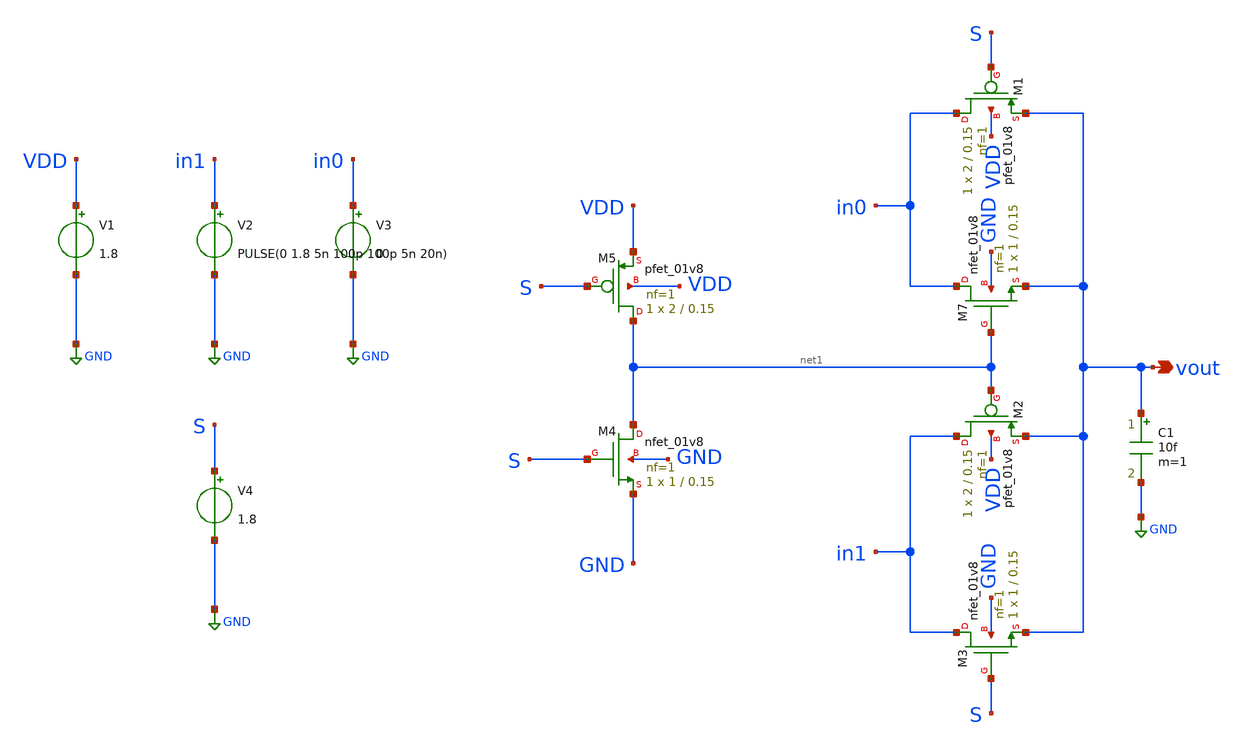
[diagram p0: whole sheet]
** sch_path: MUX/sky130_mux_tb.sch
**.subckt sky130_mux_tb vout
*.opin vout
XM1 in0 S vout VDD sky130_fd_pr__pfet_01v8 L=0.15 W=2 nf=1 ad='int((1 + 1)/2) * 2 / 1 * 0.29' as='int((1 + 2)/2) * 2 / 1 * 0.29'
+ pd='2*int((1 + 1)/2) * (2 / 1 + 0.29)' ps='2*int((1 + 2)/2) * (2 / 1 + 0.29)' nrd='0.29 / 2 ' nrs='0.29 / 2 '
+ sa=0 sb=0 sd=0 mult=1 m=1
XM2 in1 net1 vout VDD sky130_fd_pr__pfet_01v8 L=0.15 W=2 nf=1 ad='int((1 + 1)/2) * 2 / 1 * 0.29' as='int((1 + 2)/2) * 2 / 1 * 0.29'
+ pd='2*int((1 + 1)/2) * (2 / 1 + 0.29)' ps='2*int((1 + 2)/2) * (2 / 1 + 0.29)' nrd='0.29 / 2 ' nrs='0.29 / 2 '
+ sa=0 sb=0 sd=0 mult=1 m=1
XM5 net1 S VDD VDD sky130_fd_pr__pfet_01v8 L=0.15 W=2 nf=1 ad='int((1 + 1)/2) * 2 / 1 * 0.29' as='int((1 + 2)/2) * 2 / 1 * 0.29'
+ pd='2*int((1 + 1)/2) * (2 / 1 + 0.29)' ps='2*int((1 + 2)/2) * (2 / 1 + 0.29)' nrd='0.29 / 2 ' nrs='0.29 / 2 '
+ sa=0 sb=0 sd=0 mult=1 m=1
XM7 in0 net1 vout GND sky130_fd_pr__nfet_01v8 L=0.15 W=1 nf=1 ad='int((1 + 1)/2) * 1 / 1 * 0.29' as='int((1 + 2)/2) * 1 / 1 * 0.29'
+ pd='2*int((1 + 1)/2) * (1 / 1 + 0.29)' ps='2*int((1 + 2)/2) * (1 / 1 + 0.29)' nrd='0.29 / 1 ' nrs='0.29 / 1 '
+ sa=0 sb=0 sd=0 mult=1 m=1
XM3 in1 S vout GND sky130_fd_pr__nfet_01v8 L=0.15 W=1 nf=1 ad='int((1 + 1)/2) * 1 / 1 * 0.29' as='int((1 + 2)/2) * 1 / 1 * 0.29'
+ pd='2*int((1 + 1)/2) * (1 / 1 + 0.29)' ps='2*int((1 + 2)/2) * (1 / 1 + 0.29)' nrd='0.29 / 1 ' nrs='0.29 / 1 '
+ sa=0 sb=0 sd=0 mult=1 m=1
XM4 net1 S GND GND sky130_fd_pr__nfet_01v8 L=0.15 W=1 nf=1 ad='int((1 + 1)/2) * 1 / 1 * 0.29' as='int((1 + 2)/2) * 1 / 1 * 0.29'
+ pd='2*int((1 + 1)/2) * (1 / 1 + 0.29)' ps='2*int((1 + 2)/2) * (1 / 1 + 0.29)' nrd='0.29 / 1 ' nrs='0.29 / 1 '
+ sa=0 sb=0 sd=0 mult=1 m=1
V1 VDD GND 1.8
V2 in1 GND PULSE(0 1.8 5n 100p 100p 5n 20n)
V3 in0 GND 0
V4 S GND 1.8
C1 vout GND 10f m=1
**** begin user architecture code


.lib /opt/pdk/share/pdk/sky130A/libs.tech/ngspice/sky130.lib.spice tt

.temp 25

*** ========================================
*** TEST 1: INPUT SELECTION - DISABLED
*** Sources: V1=1.8, V2=1.8, V3=0.2
*** V4=PULSE(0 1.8 1n 100p 100p 5n 10n)
*** ========================================
*** .control
*** save all
*** tran 10p 50n
*** plot v(in0) v(in1) v(S)+2 v(vout)+4
*** write tg_mux.raw
*** .endc

*** ========================================
*** TEST 2: IN0 DELAY - DISABLED
*** Sources: V1=1.8, V2=0, V4=0
*** V3=PULSE(0 1.8 5n 100p 100p 5n 20n)
*** ========================================
***.control
***ave all
***tran 1p 12n 0 1p
***meas tran tplh trig v(in0) val=0.9 rise=1 targ v(vout) val=0.9 rise=1
***meas tran tphl trig v(in0) val=0.9 fall=1 targ v(vout) val=0.9 fall=1
***let tplh_ps=tplh*1e12
***let tphl_ps=tphl*1e12
***print tplh_ps tphl_ps
***write tg_mux_delay.raw
***.endc

*** ========================================
*** TEST 3: IN1 DELAY - ACTIVE
*** Sources: V1=1.8, V3=0, V4=1.8
*** V2=PULSE(0 1.8 5n 100p 100p 5n 20n)
*** ========================================
.control
save all
tran 1p 12n 0 1p

meas tran tplh trig v(in1) val=0.9 rise=1 targ v(vout) val=0.9 rise=1
meas tran tphl trig v(in1) val=0.9 fall=1 targ v(vout) val=0.9 fall=1

let tplh_ps=tplh*1e12
let tphl_ps=tphl*1e12
print tplh_ps tphl_ps

write tg_mux_delay_in1.raw
.endc


**** end user architecture code
**.ends
.GLOBAL GND
.end
